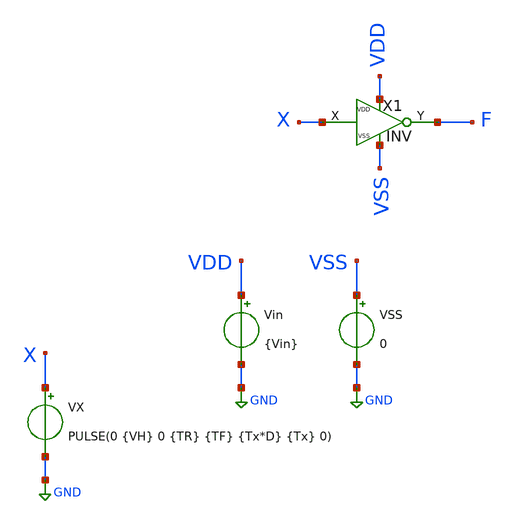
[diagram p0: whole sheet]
** sch_path: xschem/DigitalGates/TB_INV.sch
**.subckt TB_INV
Vin VDD GND {Vin}
VX X GND PULSE(0 {VH} 0 {TR} {TF} {Tx*D} {Tx} 0)
VSS VSS GND 0
X1 X F VDD VSS INV
**** begin user architecture code


.param Vin = 1.2
.param VH = 1.2
.param Del = 0

*.param fsw = 10Meg
*.param fsw = 8.4Meg
.param fsw = 1Meg

.param Tx = 1/fsw
.param Ty = Tx/5
.param D = 0.5
.param TR = 1n
.param TF = 1n
.param TdR = 0.5n
.param TdF = 0.5n

*.option temp = 125
*.option temp = -40
.option temp = 27





.save all
.param SimTime = 5*Tx
.csparam Sim_end = {SimTime}
*.csparam T = {T}

.tran 1n {SimTime} uic

.control
run
*meas tran P_M2_mean AVG P_M2 FROM={Tmeas_i} TO={Tmeas_end}

plot v(X) v(F)+2
*write TB_DCDCBuck.raw
.endc


.end




.param temp=27
.param mult = 1

.param w_INV =0.15u
.param l_INV = 0.15u

.param w_INV =0.15u
.param l_INV =0.15u








.lib cornerMOShv.lib mos_tt
.lib cornerMOSlv.lib mos_tt
*.lib cornerMOShv.lib mos_ff
*.lib cornerMOSlv.lib mos_ff
*.lib cornerMOShv.lib mos_ss
*.lib cornerMOSlv.lib mos_ss
*.lib cornerMOShv.lib mos_sf
*.lib cornerMOSlv.lib mos_sf
*.lib cornerMOShv.lib mos_fs
*.lib cornerMOSlv.lib mos_fs

*.include /opt/pdks/ihp-sg13g2/libs.ref/sg13g2_stdcell/spice/sg13g2_stdcell.spice
*.lib $::SG13G2_MODELS/cornerRES.lib res_typ
*.lib $::SG13G2_MODELS/cornerCAP.lib cap_typ
*.lib $::SG13G2_MODELS/diodes.lib




**** end user architecture code
**.ends

* expanding   symbol:  ../DigitalGates/INV.sym # of pins=4
** sym_path: xschem/DigitalGates/INV.sym
** sch_path: xschem/DigitalGates/INV.sch
.subckt INV X Y VDD VSS
*.iopin VDD
*.ipin X
*.opin Y
*.iopin VSS
XM3 Y X VSS VSS sg13_lv_nmos w={w_inv} l={l_inv} ng=1 m={mult} mm_ok=1
XM4 Y X VDD VDD sg13_lv_pmos w={w_inv} l={l_inv} ng=1 m={mult*3} mm_ok=1
**** begin user architecture code



**** end user architecture code
.ends

.GLOBAL GND
.end
